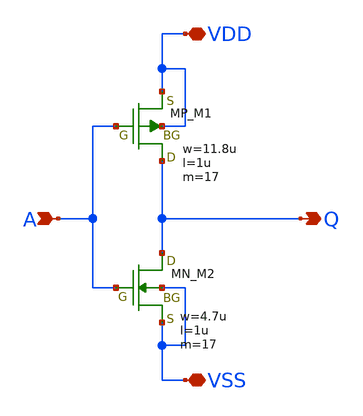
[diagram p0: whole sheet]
** sch_path: member_project/ringOSC/noritsuna/inverter_ssk.sch
**.subckt inverter_ssk A VDD Q VSS
*.ipin A
*.iopin VDD
*.opin Q
*.iopin VSS
XM1 Q A VDD VDD PMOS w=11.8u l=1u as=0 ad=0 ps=0 pd=0 nrd=0 nrs=0 m=17
XM2 Q A VSS VSS NMOS w=4.7u l=1u as=0 ad=0 ps=0 pd=0 nrd=0 nrs=0 m=17
**.ends
.end
